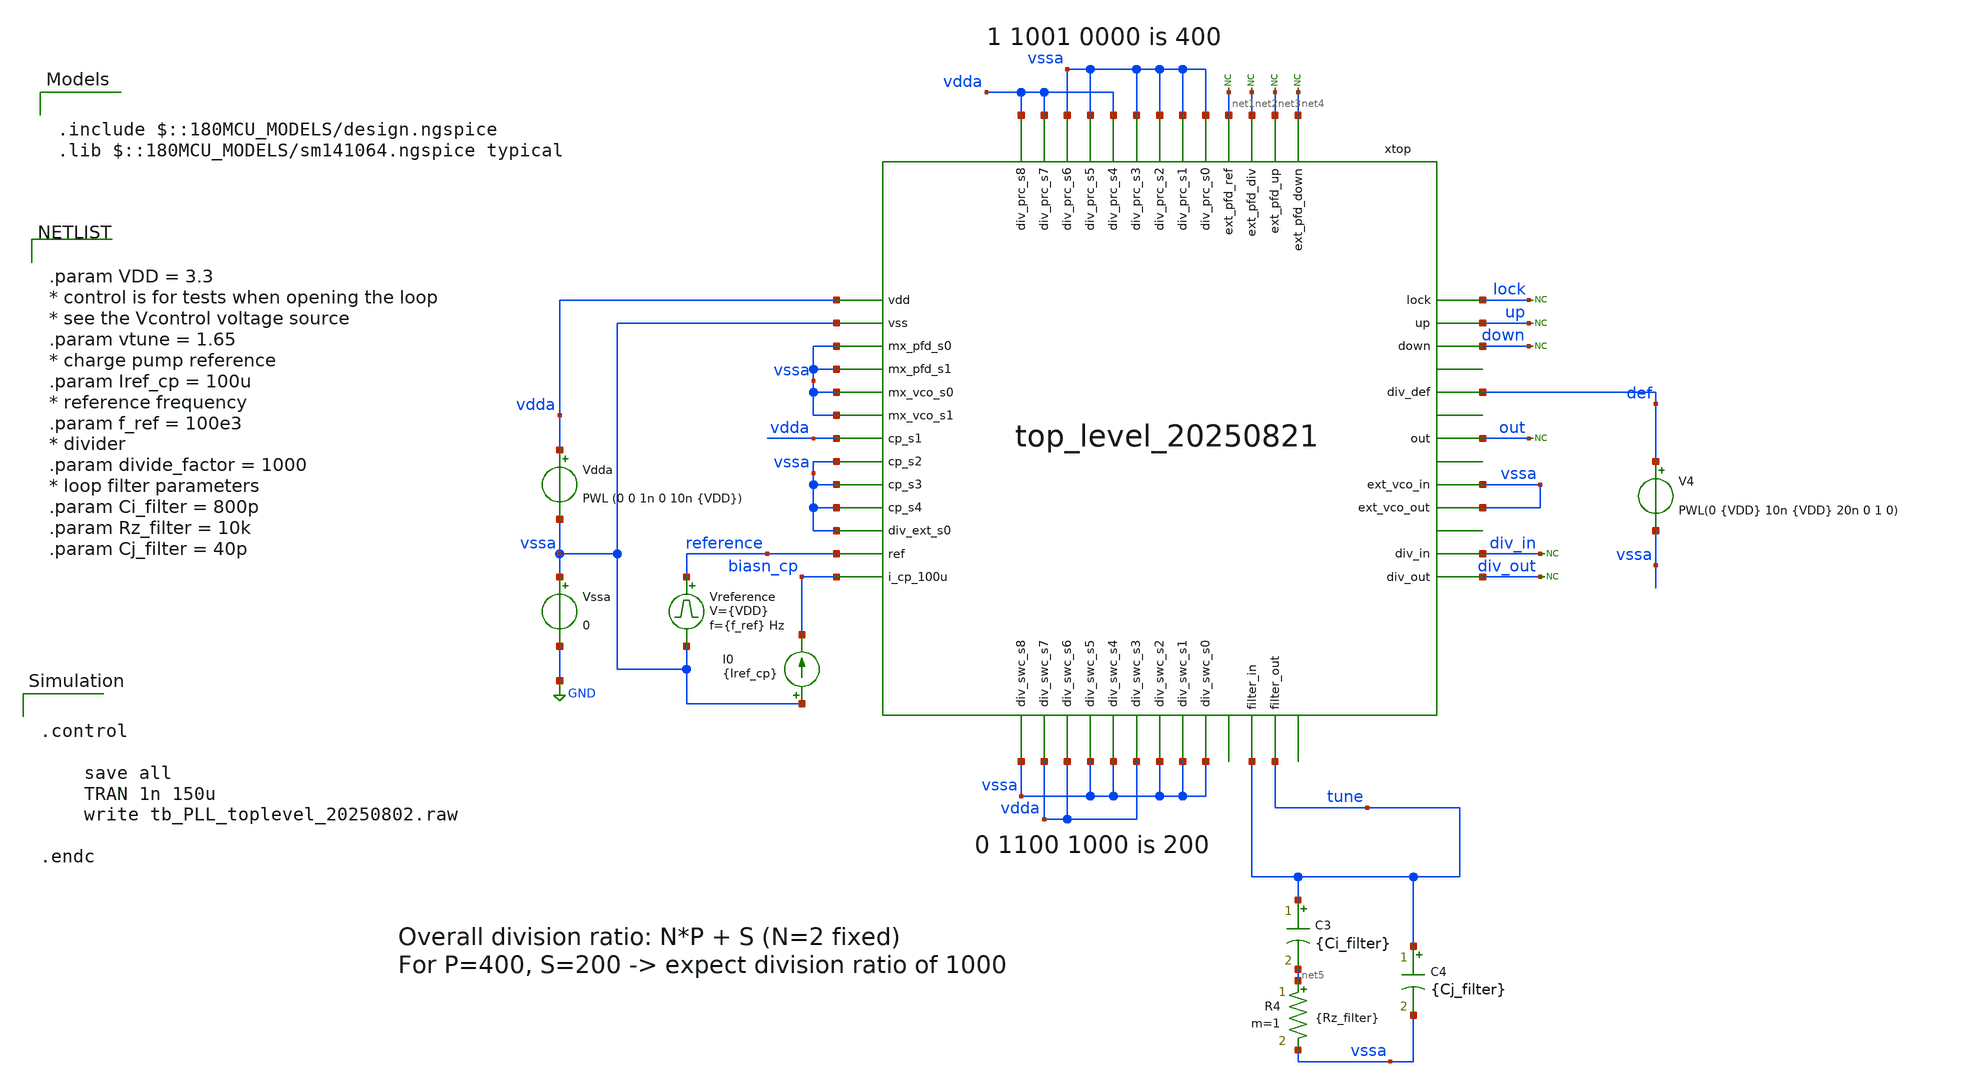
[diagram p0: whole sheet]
** sch_path: designs/libs/tb_top_level/tb_top_level_20250821.sch
**.subckt tb_top_level_20250821
Vreference reference vssa pulse 0 {VDD} '0.495/ {f_ref} ' '0.01/{f_ref} ' '0.01/{f_ref} ' '0.49/{f_ref} '
+ '1/{f_ref} '
Vssa vssa GND 0
Vdda vdda vssa PWL (0 0 1n 0 10n {VDD})
I0 vssa biasn_cp {Iref_cp}
V4 def vssa PWL(0 {VDD} 10n {VDD} 20n 0 1 0)
xtop vdda vssa vssa vssa vssa vssa vssa vdda vssa vssa vssa vssa vdda vdda vssa vssa vdda vssa vssa
+ vssa vdda vdda vssa vssa vdda vssa vssa vssa vssa reference biasn_cp net1 net2 net3 net4 lock up down
+ tune vssa div_in div_out out tune vssa def top_level_20250821
* noconn #net1
* noconn #net2
* noconn #net3
* noconn #net4
* noconn div_in
* noconn div_out
* noconn down
* noconn up
* noconn lock
C3 tune net5 {Ci_filter} m=1
R4 net5 vssa {Rz_filter} m=1
C4 tune vssa {Cj_filter} m=1
* noconn out
**** begin user architecture code


.control

    save all
    TRAN 1n 150u
    write tb_PLL_toplevel_20250802.raw

.endc




.param VDD = 3.3
* control is for tests when opening the loop
* see the Vcontrol voltage source
.param vtune = 1.65
* charge pump reference
.param Iref_cp = 100u
* reference frequency
.param f_ref = 100e3
* divider
.param divide_factor = 1000
* loop filter parameters
.param Ci_filter = 800p
.param Rz_filter = 10k
.param Cj_filter = 40p



.include $::180MCU_MODELS/design.ngspice
.lib $::180MCU_MODELS/sm141064.ngspice typical

**** end user architecture code
**.ends
.GLOBAL GND
.end
